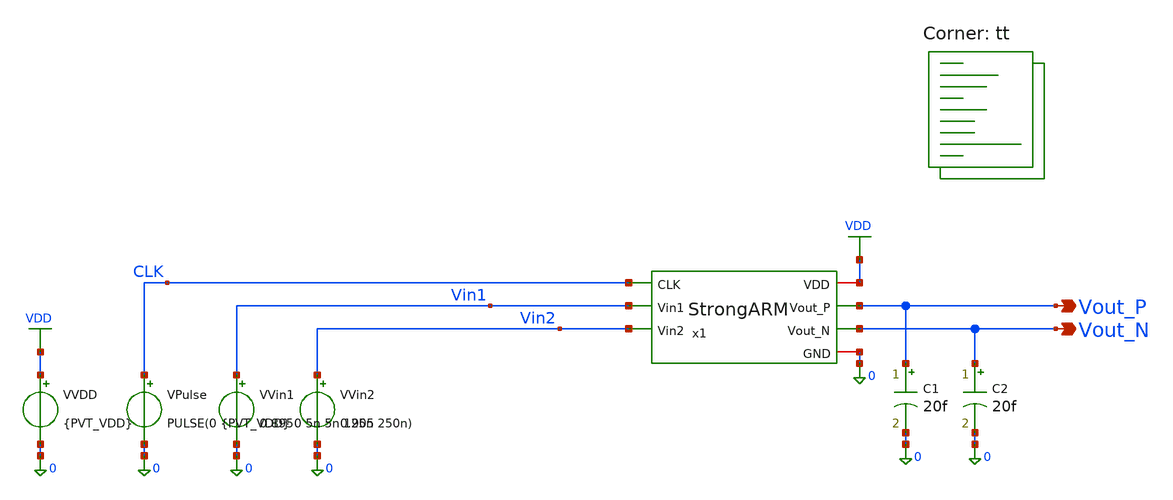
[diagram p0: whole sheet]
** sch_path: blocks/03_StrongARM/sim/tb_StrongARM_PVT.sch
**.subckt tb_StrongARM_PVT Vout_P Vout_N
*.opin Vout_P
*.opin Vout_N
x1 VDD CLK Vout_P Vout_N Vin1 Vin2 0 StrongARM
VVDD VDD 0 {PVT_VDD}
VVin1 Vin1 0 0.895
VVin2 Vin2 0 0.905
VPulse CLK 0 PULSE(0 {PVT_VDD} 0 5n 5n 125n 250n)
C1 Vout_P 0 20f m=1
C2 Vout_N 0 20f m=1
**** begin user architecture code
.lib $::SKYWATER_MODELS/sky130.lib.spice tt



* ==========================================
* BLOCK 3 - STRONGARM COMPARATOR
* TEST 8 - AUTOMATED PVT VERIFICATION
* SKY130 / 4MHz / 20fF OUTPUT LOADS
* VDD: 1.62 / 1.80 / 1.90 V
* TEMP: -40 / 27 / 125 CELSIUS
* VIN COMMON MODE: FIXED 0.9 V
* ==========================================

.param PVT_VDD=1.8

.control
save all

echo ==========================================
echo STRONGARM AUTOMATED PVT VERIFICATION
echo ==========================================

foreach v 1.62 1.80 1.90

  foreach temp_c -40 27 125

    * Reload the circuit with new supply
    alterparam PVT_VDD=$v
    reset

    * Apply temperature after reset
    set temp=$temp_c

    foreach dv -0.01 0.01

      setplot const

      let vip = 0.9 + ($dv / 2)
      let vin = 0.9 - ($dv / 2)

      alter VVin1 $&vip
      alter VVin2 $&vin

      echo
      echo ==========================================
      echo PVT_CASE_BEGIN
      echo VDD = $v
      echo TEMP_C = $temp_c
      echo DIFFERENTIAL_V = $dv
      echo ==========================================

      tran 0.2n 2.5u
	* Audit transistor S3

let s3_vgs = abs(v(clk)-v(vdd))
let s3_vgd = abs(v(clk)-v(vout_p))
let s3_vds = abs(v(vout_p)-v(vdd))

meas tran s3_vgs_max MAX s3_vgs FROM=1.99u TO=2.15u
meas tran s3_vgd_max MAX s3_vgd FROM=1.99u TO=2.15u
meas tran s3_vds_max MAX s3_vds FROM=1.99u TO=2.15u

      * Rail tracking verification
      meas tran supply_hi FIND v(vdd) AT=2.01u
      meas tran clk_hi FIND v(clk) AT=2.01u

      * Dynamic logic threshold: 50 percent VDD
      let vhalf = $v / 2

      * Decision delay on the expected falling side
      if $dv < 0
        meas tran decision_delay TRIG v(clk) VAL=$&vhalf RISE=9 TARG v(vout_n) VAL=$&vhalf FALL=9
      else
        meas tran decision_delay TRIG v(clk) VAL=$&vhalf RISE=9 TARG v(vout_p) VAL=$&vhalf FALL=9
      end

      * Evaluated logic levels
      meas tran vp_eval FIND v(vout_p) AT=2.01u
      meas tran vn_eval FIND v(vout_n) AT=2.01u

      * Later decision check
      meas tran vp_late FIND v(vout_p) AT=2.08u
      meas tran vn_late FIND v(vout_n) AT=2.08u

      * Reset verification
      meas tran vp_reset FIND v(vout_p) AT=2.20u
      meas tran vn_reset FIND v(vout_n) AT=2.20u

      * Supply current
      meas tran ivdd_avg AVG i(VVDD) FROM=500n TO=2.5u

      * Power and energy
      let power_uw = -$v * ivdd_avg * 1e6
      let energy_pj = power_uw / 4

      * Decision time
      let delay_ns = decision_delay * 1e9

      echo ==========================================
      echo PVT TIMING
      echo ==========================================
      print delay_ns

      echo ==========================================
      echo PVT POWER
      echo ==========================================
      print power_uw
      print energy_pj

      echo ==========================================
      echo OUTPUT EXTREMA
      echo ==========================================

      meas tran vp_max MAX v(vout_p) FROM=500n TO=2.5u
      meas tran vp_min MIN v(vout_p) FROM=500n TO=2.5u

      meas tran vn_max MAX v(vout_n) FROM=500n TO=2.5u
      meas tran vn_min MIN v(vout_n) FROM=500n TO=2.5u

      echo ==========================================
      echo PVT_CASE_END
      echo ==========================================

    end

  end

end

echo
echo ==========================================
echo ALL 18 PVT CASES COMPLETED
echo ==========================================
echo

.endc

**** end user architecture code
**.ends

* expanding   symbol:  blocks/03_StrongARM/xschem/StrongARM.sym # of pins=7
** sym_path: blocks/03_StrongARM/xschem/StrongARM.sym
** sch_path: blocks/03_StrongARM/xschem/StrongARM.sch
.subckt StrongARM VDD CLK Vout_P Vout_N Vin1 Vin2 GND
*.iopin VDD
*.iopin GND
*.ipin Vin1
*.ipin Vin2
*.ipin CLK
*.opin Vout_P
*.opin Vout_N
XS1 P CLK VDD VDD sky130_fd_pr__pfet_01v8 L=0.15 W=1.5 nf=1 ad='int((1 + 1)/2) * 1.5 / 1 * 0.29' as='int((1 + 2)/2) * 1.5 / 1 * 0.29'
+ pd='2*int((1 + 1)/2) * (1.5 / 1 + 0.29)' ps='2*int((1 + 2)/2) * (1.5 / 1 + 0.29)' nrd='0.29 / 1.5 ' nrs='0.29 / 1.5 '
+ sa=0 sb=0 sd=0 mult=1 m=1
XS3 Vout_P CLK VDD VDD sky130_fd_pr__pfet_01v8 L=0.15 W=1.5 nf=1 ad='int((1 + 1)/2) * 1.5 / 1 * 0.29'
+ as='int((1 + 2)/2) * 1.5 / 1 * 0.29' pd='2*int((1 + 1)/2) * (1.5 / 1 + 0.29)' ps='2*int((1 + 2)/2) * (1.5 / 1 + 0.29)'
+ nrd='0.29 / 1.5 ' nrs='0.29 / 1.5 ' sa=0 sb=0 sd=0 mult=1 m=1
XM5 Vout_P Vout_N VDD VDD sky130_fd_pr__pfet_01v8 L=0.3 W=5 nf=1 ad='int((1 + 1)/2) * 5 / 1 * 0.29' as='int((1 + 2)/2) * 5 / 1 * 0.29'
+ pd='2*int((1 + 1)/2) * (5 / 1 + 0.29)' ps='2*int((1 + 2)/2) * (5 / 1 + 0.29)' nrd='0.29 / 5 ' nrs='0.29 / 5 '
+ sa=0 sb=0 sd=0 mult=1 m=1
XM6 Vout_N Vout_P VDD VDD sky130_fd_pr__pfet_01v8 L=0.3 W=5 nf=1 ad='int((1 + 1)/2) * 5 / 1 * 0.29' as='int((1 + 2)/2) * 5 / 1 * 0.29'
+ pd='2*int((1 + 1)/2) * (5 / 1 + 0.29)' ps='2*int((1 + 2)/2) * (5 / 1 + 0.29)' nrd='0.29 / 5 ' nrs='0.29 / 5 '
+ sa=0 sb=0 sd=0 mult=1 m=1
XS4 Vout_N CLK VDD VDD sky130_fd_pr__pfet_01v8 L=0.15 W=1.5 nf=1 ad='int((1 + 1)/2) * 1.5 / 1 * 0.29'
+ as='int((1 + 2)/2) * 1.5 / 1 * 0.29' pd='2*int((1 + 1)/2) * (1.5 / 1 + 0.29)' ps='2*int((1 + 2)/2) * (1.5 / 1 + 0.29)'
+ nrd='0.29 / 1.5 ' nrs='0.29 / 1.5 ' sa=0 sb=0 sd=0 mult=1 m=1
XS2 Q CLK VDD VDD sky130_fd_pr__pfet_01v8 L=0.15 W=1.5 nf=1 ad='int((1 + 1)/2) * 1.5 / 1 * 0.29' as='int((1 + 2)/2) * 1.5 / 1 * 0.29'
+ pd='2*int((1 + 1)/2) * (1.5 / 1 + 0.29)' ps='2*int((1 + 2)/2) * (1.5 / 1 + 0.29)' nrd='0.29 / 1.5 ' nrs='0.29 / 1.5 '
+ sa=0 sb=0 sd=0 mult=1 m=1
XM3 Vout_P Vout_N P GND sky130_fd_pr__nfet_01v8 L=0.3 W=2 nf=1 ad='int((1 + 1)/2) * 2 / 1 * 0.29' as='int((1 + 2)/2) * 2 / 1 * 0.29'
+ pd='2*int((1 + 1)/2) * (2 / 1 + 0.29)' ps='2*int((1 + 2)/2) * (2 / 1 + 0.29)' nrd='0.29 / 2 ' nrs='0.29 / 2 '
+ sa=0 sb=0 sd=0 mult=1 m=1
XM4 Vout_N Vout_P Q GND sky130_fd_pr__nfet_01v8 L=0.3 W=2 nf=1 ad='int((1 + 1)/2) * 2 / 1 * 0.29' as='int((1 + 2)/2) * 2 / 1 * 0.29'
+ pd='2*int((1 + 1)/2) * (2 / 1 + 0.29)' ps='2*int((1 + 2)/2) * (2 / 1 + 0.29)' nrd='0.29 / 2 ' nrs='0.29 / 2 '
+ sa=0 sb=0 sd=0 mult=1 m=1
XM1 P Vin1 TAIL GND sky130_fd_pr__nfet_01v8 L=0.5 W=10 nf=1 ad='int((1 + 1)/2) * 10 / 1 * 0.29' as='int((1 + 2)/2) * 10 / 1 * 0.29'
+ pd='2*int((1 + 1)/2) * (10 / 1 + 0.29)' ps='2*int((1 + 2)/2) * (10 / 1 + 0.29)' nrd='0.29 / 10 ' nrs='0.29 / 10 '
+ sa=0 sb=0 sd=0 mult=1 m=1
XM2 Q Vin2 TAIL GND sky130_fd_pr__nfet_01v8 L=0.5 W=10 nf=1 ad='int((1 + 1)/2) * 10 / 1 * 0.29' as='int((1 + 2)/2) * 10 / 1 * 0.29'
+ pd='2*int((1 + 1)/2) * (10 / 1 + 0.29)' ps='2*int((1 + 2)/2) * (10 / 1 + 0.29)' nrd='0.29 / 10 ' nrs='0.29 / 10 '
+ sa=0 sb=0 sd=0 mult=1 m=1
XM7 TAIL CLK GND GND sky130_fd_pr__nfet_01v8 L=0.3 W=1 nf=1 ad='int((1 + 1)/2) * 1 / 1 * 0.29' as='int((1 + 2)/2) * 1 / 1 * 0.29'
+ pd='2*int((1 + 1)/2) * (1 / 1 + 0.29)' ps='2*int((1 + 2)/2) * (1 / 1 + 0.29)' nrd='0.29 / 1 ' nrs='0.29 / 1 '
+ sa=0 sb=0 sd=0 mult=1 m=1
.ends

.GLOBAL VDD
.end
